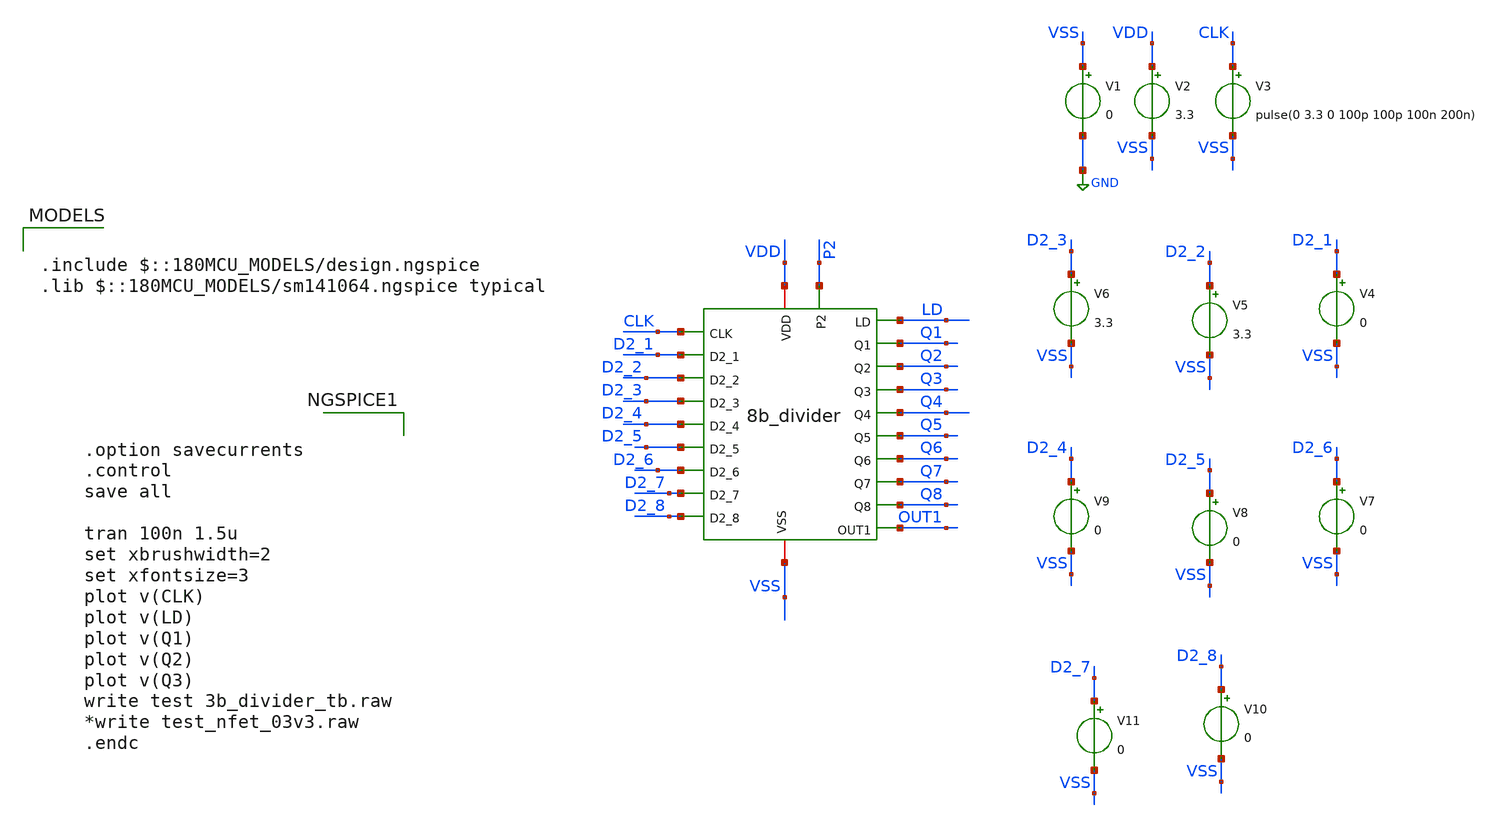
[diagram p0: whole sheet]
** sch_path: Clock_Generator_PAKISTAN_06/Xschem/untitled-9.sch
**.subckt untitled-9
x1 VDD LD CLK D2_1 Q1 D2_2 Q2 D2_3 Q3 D2_4 Q4 D2_5 Q5 D2_6 Q6 D2_7 Q7 D2_8 Q8 VSS OUT1 P2 8b_divider
V1 VSS GND 0
V2 VDD VSS 3.3
V3 CLK VSS pulse(0 3.3 0 100p 100p 100n 200n)
V4 D2_1 VSS 0
V5 D2_2 VSS 3.3
V6 D2_3 VSS 3.3
V7 D2_6 VSS 0
V8 D2_5 VSS 0
V9 D2_4 VSS 0
V10 D2_8 VSS 0
V11 D2_7 VSS 0
**** begin user architecture code

.include $::180MCU_MODELS/design.ngspice
.lib $::180MCU_MODELS/sm141064.ngspice typical



.option savecurrents
.control
save all

tran 100n 1.5u
set xbrushwidth=2
set xfontsize=3
plot v(CLK)
plot v(LD)
plot v(Q1)
plot v(Q2)
plot v(Q3)
write test 3b_divider_tb.raw
*write test_nfet_03v3.raw
.endc


**** end user architecture code
**.ends
.GLOBAL GND
.end
